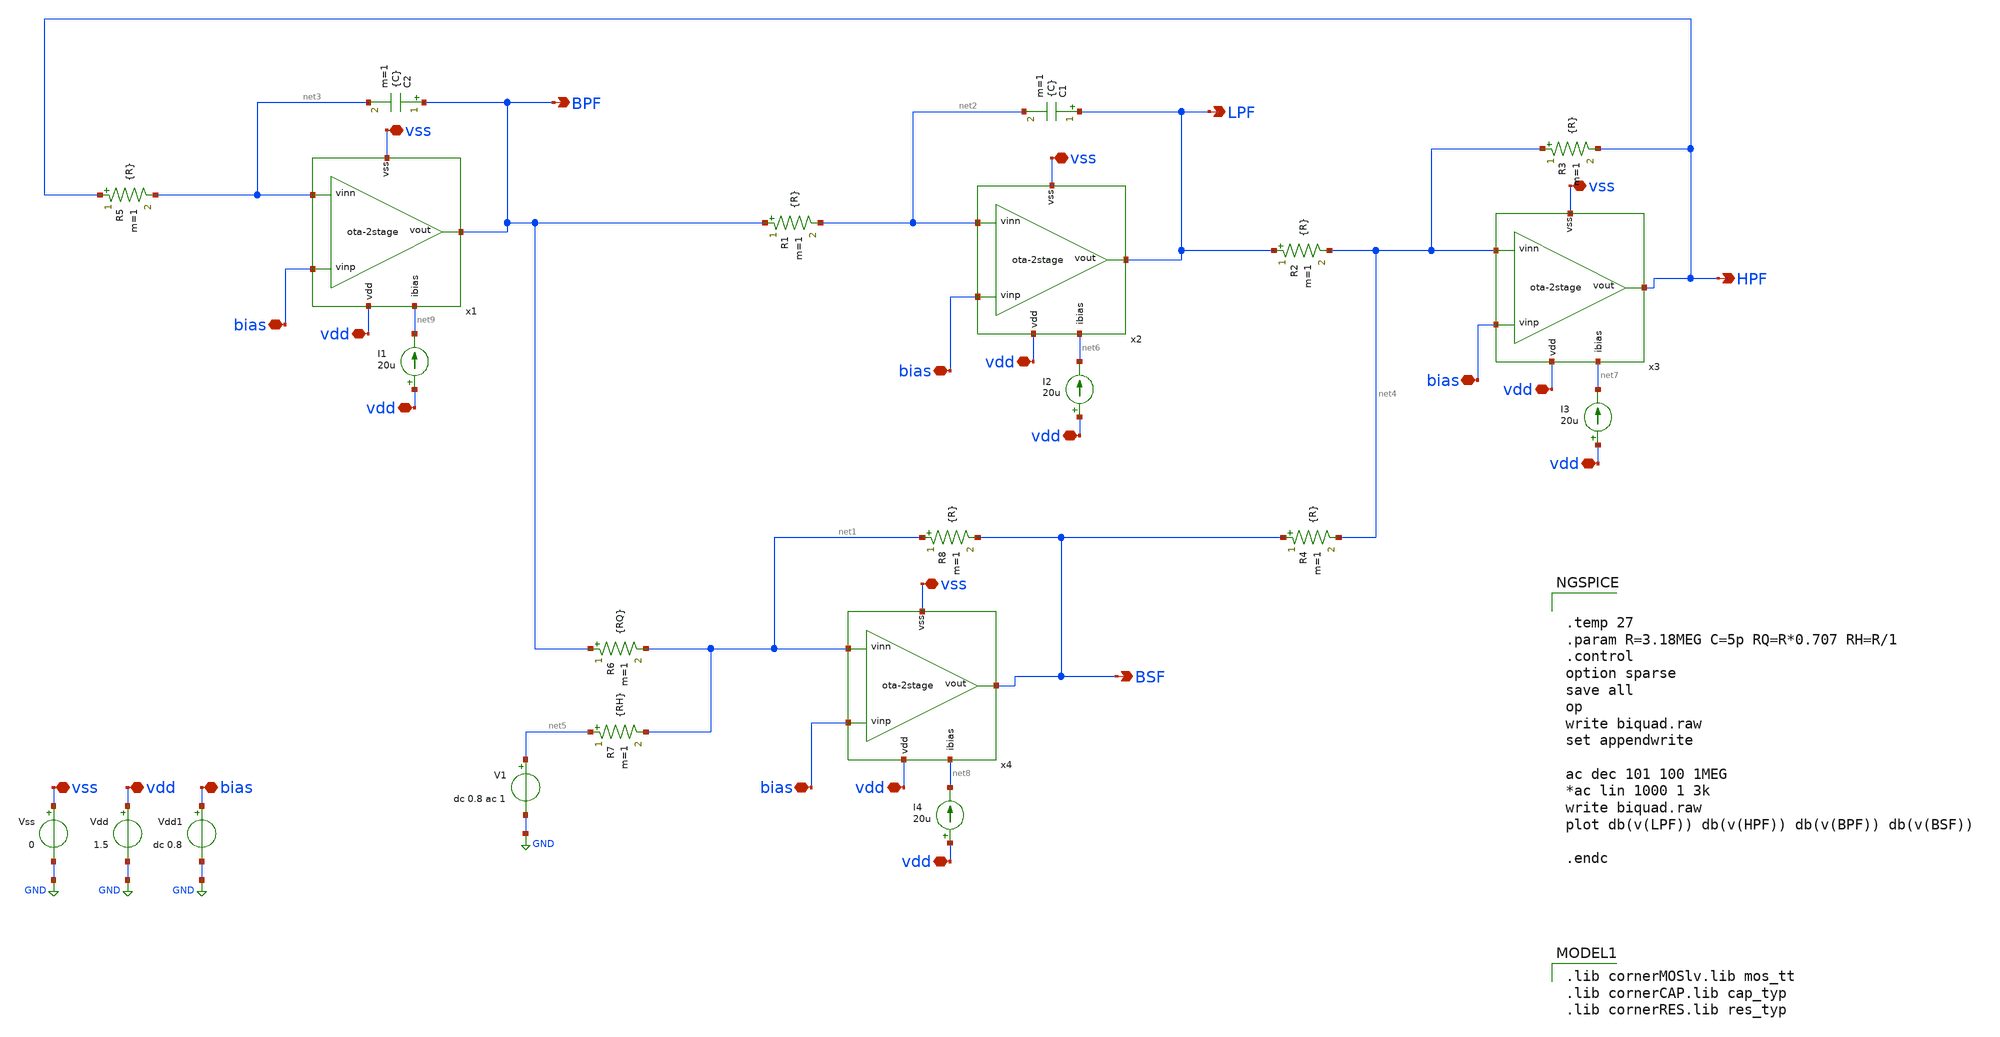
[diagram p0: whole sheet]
** sch_path: teshbench/2stage-ota_tb-biquad_univ.sch
**.subckt 2stage-ota_tb-biquad_univ HPF BSF LPF BPF vss vdd vdd vss vdd vss vss vdd vdd bias bias
*+ bias bias bias vss vdd vdd vdd vdd
*.opin HPF
*.opin BSF
*.opin LPF
*.opin BPF
*.iopin vss
*.iopin vdd
*.iopin vdd
*.iopin vss
*.iopin vdd
*.iopin vss
*.iopin vss
*.iopin vdd
*.iopin vdd
*.iopin bias
*.iopin bias
*.iopin bias
*.iopin bias
*.iopin bias
*.iopin vss
*.iopin vdd
*.iopin vdd
*.iopin vdd
*.iopin vdd
C1 LPF net2 {C} m=1
C2 BPF net3 {C} m=1
R1 BPF net2 {R} m=1
R2 LPF net4 {R} m=1
R3 net4 HPF {R} m=1
R4 BSF net4 {R} m=1
R5 HPF net3 {R} m=1
R6 BPF net1 {RQ} m=1
R7 net5 net1 {RH} m=1
R8 net1 BSF {R} m=1
V1 net5 GND dc 0.8 ac 1
x1 vdd net9 net3 BPF bias vss ota-2stage
Vdd vdd GND 1.5
Vss vss GND 0
x2 vdd net6 net2 LPF bias vss ota-2stage
x3 vdd net7 net4 HPF bias vss ota-2stage
x4 vdd net8 net1 BSF bias vss ota-2stage
Vdd1 bias GND dc 0.8
I1 vdd net9 20u
I2 vdd net6 20u
I3 vdd net7 20u
I4 vdd net8 20u
**** begin user architecture code


.temp 27
.param R=3.18MEG C=5p RQ=R*0.707 RH=R/1
.control
option sparse
save all
op
write biquad.raw
set appendwrite

ac dec 101 100 1MEG
*ac lin 1000 1 3k
write biquad.raw
plot db(v(LPF)) db(v(HPF)) db(v(BPF)) db(v(BSF))

.endc


 .lib cornerMOSlv.lib mos_tt
.lib cornerCAP.lib cap_typ
.lib cornerRES.lib res_typ

**** end user architecture code
**.ends
.GLOBAL GND
.end
